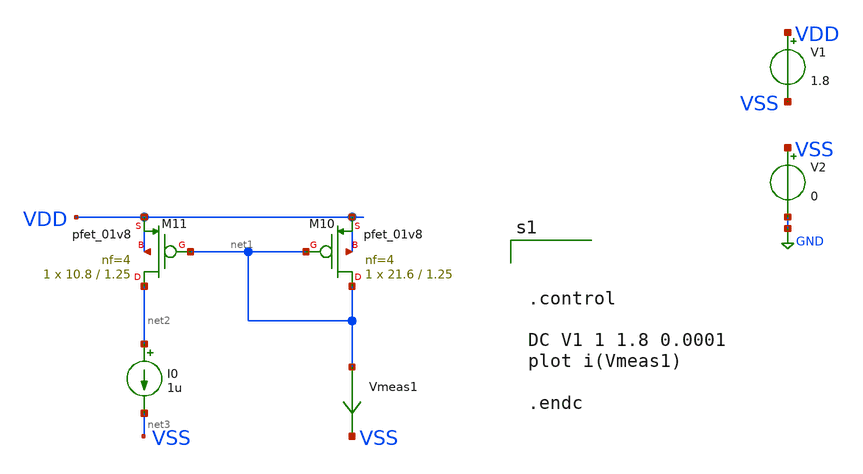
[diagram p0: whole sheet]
** sch_path: bandgap-final/bias-net/kontol.sch
**.subckt kontol
V1 net4 VSS 1.8
V2 net5 GND 0
XM10 net1 net1 VDD VDD sky130_fd_pr__pfet_01v8 L=1.25 W=21.6 nf=4 ad='int((nf+1)/2) * W/nf * 0.29' as='int((nf+2)/2) * W/nf * 0.29'
+ pd='2*int((nf+1)/2) * (W/nf + 0.29)' ps='2*int((nf+2)/2) * (W/nf + 0.29)' nrd='0.29 / W' nrs='0.29 / W'
+ sa=0 sb=0 sd=0 mult=1 m=1
XM11 net2 net1 VDD VDD sky130_fd_pr__pfet_01v8 L=1.25 W=10.8 nf=4 ad='int((nf+1)/2) * W/nf * 0.29' as='int((nf+2)/2) * W/nf * 0.29'
+ pd='2*int((nf+1)/2) * (W/nf + 0.29)' ps='2*int((nf+2)/2) * (W/nf + 0.29)' nrd='0.29 / W' nrs='0.29 / W'
+ sa=0 sb=0 sd=0 mult=1 m=1
Vmeas1 net1 net6 0
.save i(vmeas1)
I0 net2 net3 1u
**** begin user architecture code



.control

DC V1 1 1.8 0.0001
plot i(Vmeas1)

.endc






** opencircuitdesign pdks install
.lib $::SKYWATER_MODELS/sky130.lib.spice tt


**** end user architecture code
**.ends
.GLOBAL GND
.end
